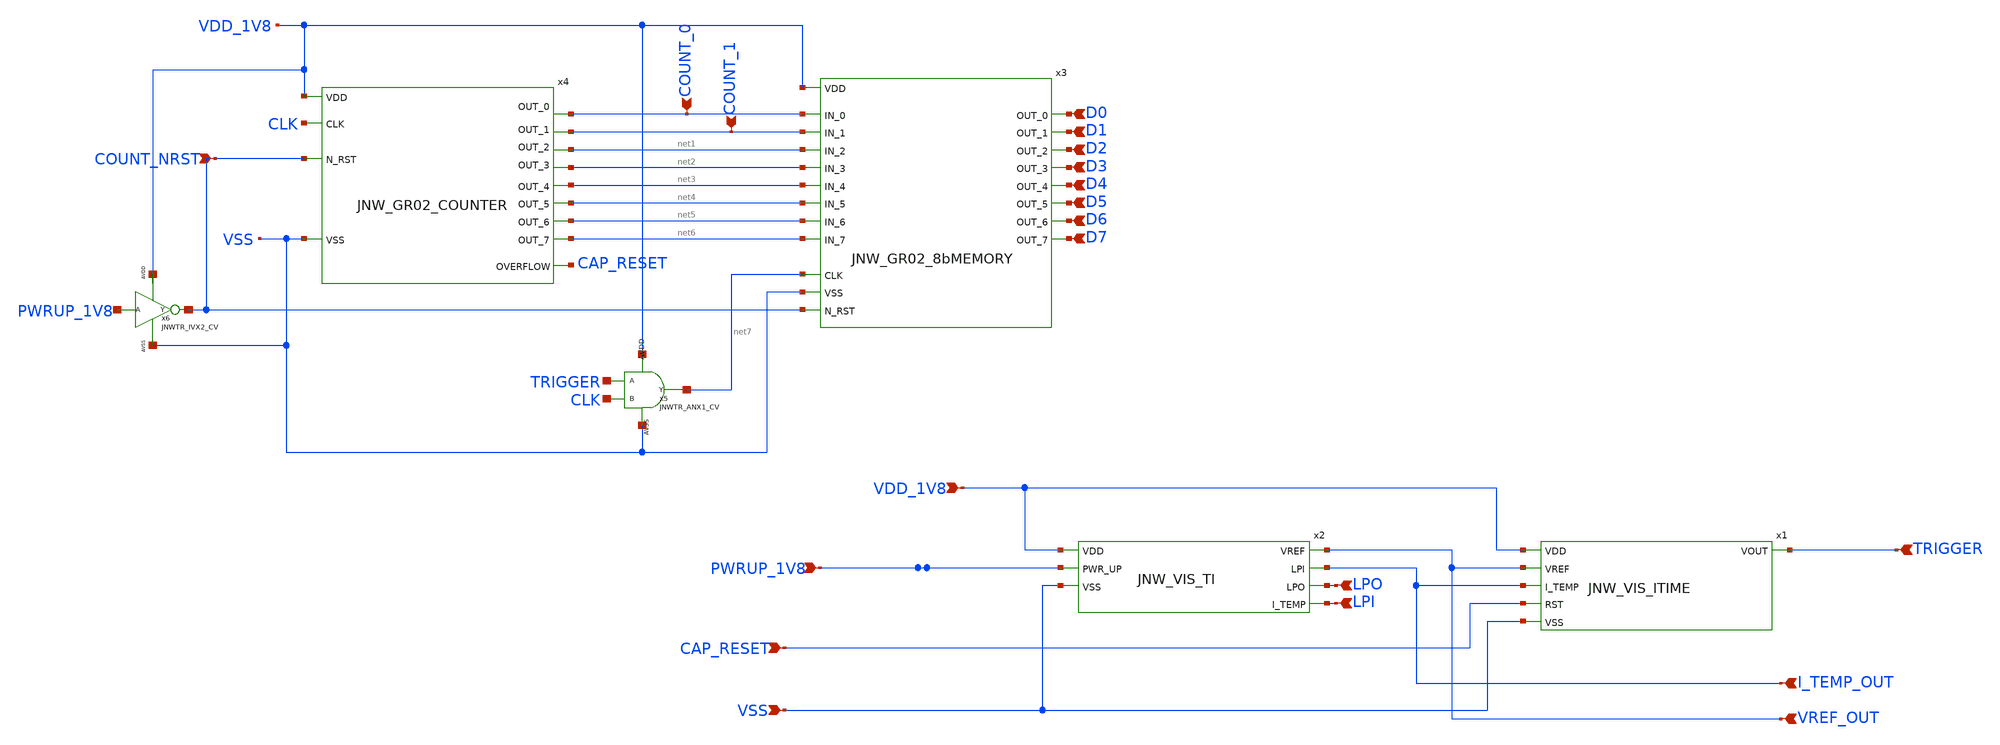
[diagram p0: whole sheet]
** sch_path: design/JNW_GR02_SKY130A/JNW_GR02_GBH_TST.sch
**.subckt JNW_GR02_GBH_TST VDD_1V8 VSS PWRUP_1V8 TRIGGER CAP_RESET I_TEMP_OUT LPI LPO VREF_OUT D0 D1
*+ D2 D3 D4 D5 D6 D7 COUNT_0 COUNT_1 COUNT_NRST
*.ipin VDD_1V8
*.ipin VSS
*.ipin PWRUP_1V8
*.ipin TRIGGER
*.ipin CAP_RESET
*.ipin I_TEMP_OUT
*.ipin LPI
*.ipin LPO
*.ipin VREF_OUT
*.ipin D0
*.ipin D1
*.ipin D2
*.ipin D3
*.ipin D4
*.ipin D5
*.ipin D6
*.ipin D7
*.ipin COUNT_0
*.ipin COUNT_1
*.ipin COUNT_NRST
x1 VDD_1V8 VREF_OUT TRIGGER I_TEMP_OUT CAP_RESET VSS JNW_VIS_ITIME
x2 VDD_1V8 VREF_OUT I_TEMP_OUT LPO LPI PWRUP_1V8 VSS JNW_VIS_TI
x3 VDD_1V8 D7 D4 COUNT_0 net1 net2 net3 net4 COUNT_1 net6 D0 D1 D2 D3 net5 D5 D6 net7 VSS COUNT_NRST
+ JNW_GR02_8bMEMORY
x4 VDD_1V8 COUNT_0 net3 net6 net5 net4 CAP_RESET net2 net1 COUNT_1 CLK VSS COUNT_NRST
+ JNW_GR02_COUNTER
x5 TRIGGER CLK net7 VDD_1V8 VSS JNWTR_ANX1_CV xoffset=0 yoffset=0 angle=0 M=1
x6 PWRUP_1V8 COUNT_NRST VDD_1V8 VSS JNWTR_IVX2_CV xoffset=0 yoffset=0 angle=0 M=1
**.ends
.end
